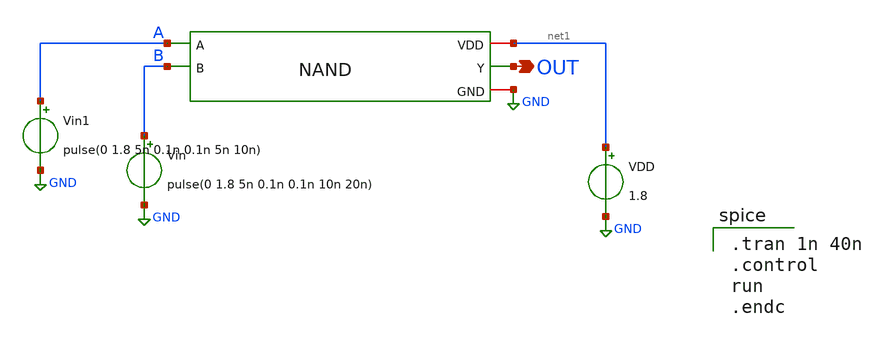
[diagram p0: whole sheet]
** sch_path: NAND/NAND_Testbench.sch
**.subckt NAND_Testbench OUT
*.opin OUT
x1 net1 A OUT B GND NAND
Vin B GND pulse(0 1.8 5n 0.1n 0.1n 10n 20n)
Vin1 A GND pulse(0 1.8 5n 0.1n 0.1n 5n 10n)
VDD net1 GND 1.8
**** begin user architecture code

.lib /usr/local/share/pdk/sky130A/libs.tech/ngspice/sky130.lib.spice tt


.tran 1n 40n
.control
run
.endc

**** end user architecture code
**.ends

* expanding   symbol:  NAND.sym # of pins=5
** sym_path: NAND/NAND.sym
** sch_path: NAND/NAND.sch
.subckt NAND VDD A Y B GND
*.ipin A
*.opin Y
*.iopin VDD
*.iopin GND
*.ipin B
XM4 Y A VDD VDD sky130_fd_pr__pfet_01v8 L=0.5 W=2 nf=1 ad='int((nf+1)/2) * W/nf * 0.29' as='int((nf+2)/2) * W/nf * 0.29'
+ pd='2*int((nf+1)/2) * (W/nf + 0.29)' ps='2*int((nf+2)/2) * (W/nf + 0.29)' nrd='0.29 / W' nrs='0.29 / W'
+ sa=0 sb=0 sd=0 mult=1 m=1
XM3 Y B VDD VDD sky130_fd_pr__pfet_01v8 L=0.5 W=2 nf=1 ad='int((nf+1)/2) * W/nf * 0.29' as='int((nf+2)/2) * W/nf * 0.29'
+ pd='2*int((nf+1)/2) * (W/nf + 0.29)' ps='2*int((nf+2)/2) * (W/nf + 0.29)' nrd='0.29 / W' nrs='0.29 / W'
+ sa=0 sb=0 sd=0 mult=1 m=1
XM2 Y B net1 GND sky130_fd_pr__nfet_01v8 L=0.5 W=2 nf=1 ad='int((nf+1)/2) * W/nf * 0.29' as='int((nf+2)/2) * W/nf * 0.29'
+ pd='2*int((nf+1)/2) * (W/nf + 0.29)' ps='2*int((nf+2)/2) * (W/nf + 0.29)' nrd='0.29 / W' nrs='0.29 / W'
+ sa=0 sb=0 sd=0 mult=1 m=1
XM1 net1 A GND GND sky130_fd_pr__nfet_01v8 L=0.5 W=2 nf=1 ad='int((nf+1)/2) * W/nf * 0.29' as='int((nf+2)/2) * W/nf * 0.29'
+ pd='2*int((nf+1)/2) * (W/nf + 0.29)' ps='2*int((nf+2)/2) * (W/nf + 0.29)' nrd='0.29 / W' nrs='0.29 / W'
+ sa=0 sb=0 sd=0 mult=1 m=1
.ends

.GLOBAL GND
.end
